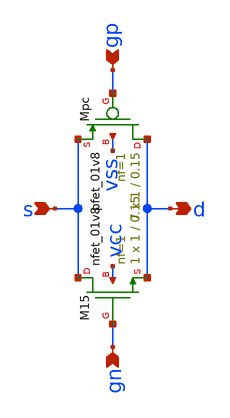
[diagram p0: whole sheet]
** sch_path: src/xe/test_cases/tgate.sch
**.subckt tgate s gp gn d
*.ipin s
*.ipin gp
*.ipin gn
*.opin d
XMpc d gp s vss sky130_fd_pr__pfet_01v8 L=0.15 W=1 nf=1 ad='int((nf+1)/2) * W/nf * 0.29' as='int((nf+2)/2) * W/nf * 0.29'
+ pd='2*int((nf+1)/2) * (W/nf + 0.29)' ps='2*int((nf+2)/2) * (W/nf + 0.29)' nrd='0.29 / W' nrs='0.29 / W'
+ sa=0 sb=0 sd=0 mult=7 m=7
XM15 s gn d vcc sky130_fd_pr__nfet_01v8 L=0.15 W=1 nf=1 ad='int((nf+1)/2) * W/nf * 0.29' as='int((nf+2)/2) * W/nf * 0.29'
+ pd='2*int((nf+1)/2) * (W/nf + 0.29)' ps='2*int((nf+2)/2) * (W/nf + 0.29)' nrd='0.29 / W' nrs='0.29 / W'
+ sa=0 sb=0 sd=0 mult=1 m=1
**.ends
.end
